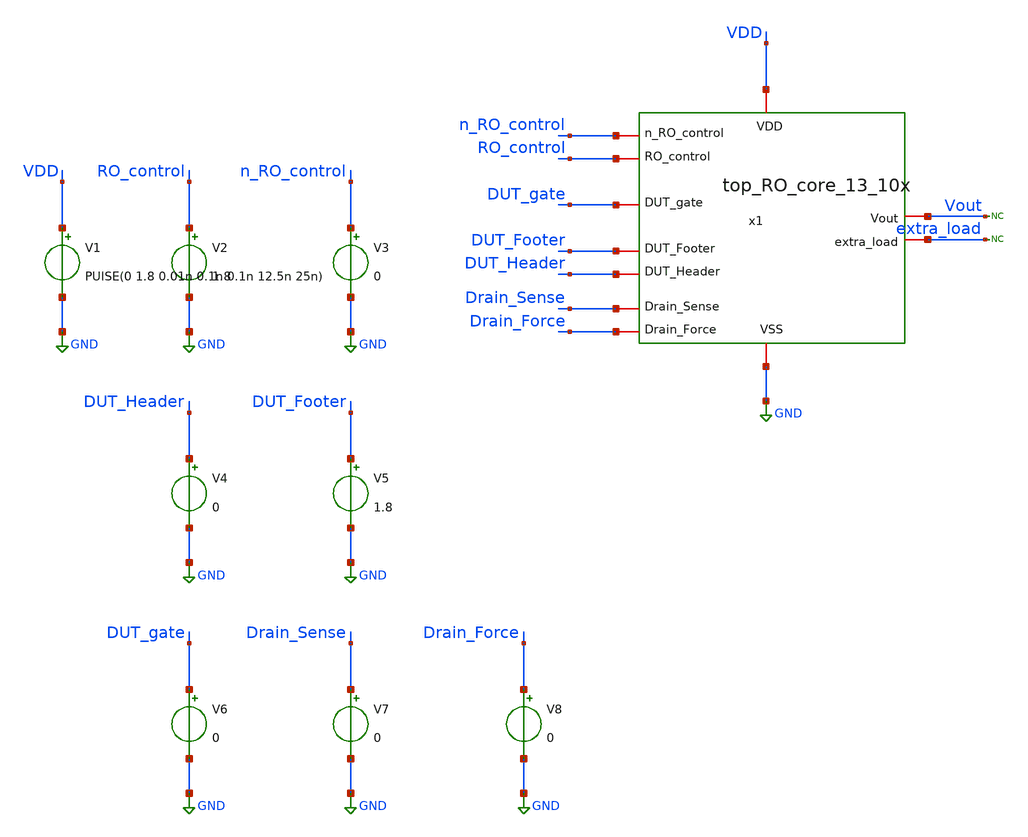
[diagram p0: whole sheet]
** sch_path: TT/top_RO_core_13_10x_tb.sch
.lib $::SKYWATER_MODELS/sky130.lib.spice tt
.include $::SKYWATER_STDCELLS/sky130_fd_sc_hd.spice

**.subckt top_RO_core_13_10x_tb
V1 VDD GND PUlSE(0 1.8 0.01n 0.1n 0.1n 12.5n 25n)
V2 RO_control GND 1.8
V3 n_RO_control GND 0
V4 DUT_Header GND 0
V5 DUT_Footer GND 1.8
* noconn extra_load
* noconn Vout
V6 DUT_gate GND 0
V7 Drain_Sense GND 0
V8 Drain_Force GND 0
x1 VDD GND n_RO_control RO_control DUT_gate Vout DUT_Header DUT_Footer Drain_Force Drain_Sense
+ extra_load top_RO_core_13_10x
**** begin user architecture code


.ic V(x1.A[8])=0.8
.tran 0.1n 50n
.save all



**** end user architecture code
**.ends

* expanding   symbol:  /foss/designs/Projects/RO_reliability/xschem/top_RO_core_13_10x.sym # of
*+ pins=11
** sym_path: TT/top_RO_core_13_10x.sym
** sch_path: TT/top_RO_core_13_10x.sch
.subckt top_RO_core_13_10x VDD VSS n_RO_control RO_control DUT_gate Vout DUT_Header DUT_Footer
+ Drain_Force Drain_Sense extra_load
*.iopin VDD
*.iopin VSS
*.iopin n_RO_control
*.iopin RO_control
*.iopin DUT_gate
*.iopin extra_load
*.iopin DUT_Header
*.iopin DUT_Footer
*.iopin Drain_Force
*.iopin Drain_Sense
*.iopin Vout
x1[1] VDD VSS A[8] A[7] rovcel2
x1[2] VDD VSS A[7] A[6] rovcel2
x1[3] VDD VSS A[6] A[5] rovcel2
x1[4] VDD VSS A[5] A[4] rovcel2
x1[5] VDD VSS A[4] A[3] rovcel2
x1[6] VDD VSS A[3] A[2] rovcel2
x1[7] VDD VSS A[2] A[1] rovcel2
x1[8] VDD VSS A[1] Vout rovcel2
x2 VDD VSS A[9] n_RO_control A_10 RO_control DUT_gate rovcel3
x3 VDD VSS A[9] A[8] rovcel2
x5 VDD VSS extra_load n_RO_control A_12 rovcel4
x6 VDD VSS Vout A_12 rovcel2
x1 DUT_Header DUT_Footer Drain_Force Drain_Sense RO_control n_RO_control VDD VSS A_10 extra_load
+ rovcel1_10
.ends


* expanding   symbol:  /foss/designs/Projects/RO_reliability/xschem/rovcel2.sym # of pins=4
** sym_path: TT/rovcel2.sym
** sch_path: TT/rovcel2.sch
.subckt rovcel2 VDD VSS Vout Vin
*.iopin VDD
*.iopin VSS
*.iopin Vin
*.iopin Vout
x1 VDD Vin Vout VSS inverter_RO_rel
x2 VDD VDD Vout net1 VSS VSS tgate
x3 VDD VDD Vout net2 VSS VSS tgate
* noconn #net1
* noconn #net2
.ends


* expanding   symbol:  /foss/designs/Projects/RO_reliability/xschem/rovcel3.sym # of pins=7
** sym_path: TT/rovcel3.sym
** sch_path: TT/rovcel3.sch
.subckt rovcel3 VDD VSS Vin n_RO_control Vout RO_control DUT_gate
*.iopin VDD
*.iopin VSS
*.iopin Vin
*.iopin n_RO_control
*.iopin RO_control
*.iopin DUT_gate
*.iopin Vout
* noconn #net1
x4 VDD VSS Vin n_RO_control RO_control Vout tristate_inv
x1 RO_control VDD Vout net1 VSS n_RO_control tgate
x5 RO_control VDD Vout DUT_gate VSS n_RO_control tgate
.ends


* expanding   symbol:  /foss/designs/Projects/RO_reliability/xschem/rovcel4.sym # of pins=5
** sym_path: TT/rovcel4.sym
** sch_path: TT/rovcel4.sch
.subckt rovcel4 VDD VSS Vin n_RO_control Vout
*.iopin VDD
*.iopin VSS
*.iopin Vin
*.iopin n_RO_control
*.iopin Vout
* noconn #net1
x4 n_RO_control VDD VSS Vin Vout inv1
x1 VDD VDD Vout VSS VSS VSS tgate
x5 VDD VDD Vout net1 VSS VSS tgate
.ends


* expanding   symbol:  /foss/designs/Projects/RO_reliability/xschem/rovcel1_10.sym # of pins=10
** sym_path: TT/rovcel1_10.sym
** sch_path: TT/rovcel1_10.sch
.subckt rovcel1_10 DUT_Header DUT_Footer Drain_Force Drain_Sense RO_control n_RO_control VDD VSS Vin
+ Vout
*.iopin VDD
*.iopin VSS
*.iopin Vin
*.iopin DUT_Header
*.iopin DUT_Footer
*.iopin Drain_Force
*.iopin Vout
*.iopin Drain_Sense
*.iopin RO_control
*.iopin n_RO_control
x1 VDD VSS Vin DUT_Header DUT_Footer Vout tristate_inv
x2 RO_control VDD Vout Drain_Sense VSS n_RO_control tgate
x3 RO_control VDD Vout Drain_Force VSS n_RO_control tgate_force10
.ends


* expanding   symbol:  /foss/designs/Projects/RO_reliability/xschem/inverter_RO_rel.sym # of pins=4
** sym_path: TT/inverter_RO_rel.sym
** sch_path: TT/inverter_RO_rel.sch
.subckt inverter_RO_rel VDD Vin Vout VSS
*.iopin VDD
*.iopin VSS
*.iopin Vin
*.iopin Vout
XM2 Vout Vin VDD VDD sky130_fd_pr__pfet_01v8 L=0.15 W=4.75 nf=1 ad='int((nf+1)/2) * W/nf * 0.29' as='int((nf+2)/2) * W/nf * 0.29'
+ pd='2*int((nf+1)/2) * (W/nf + 0.29)' ps='2*int((nf+2)/2) * (W/nf + 0.29)' nrd='0.29 / W' nrs='0.29 / W'
+ sa=0 sb=0 sd=0 mult=4 m=4
XM1 Vout Vin VSS VSS sky130_fd_pr__nfet_01v8 L=0.15 W=2.1 nf=1 ad='int((nf+1)/2) * W/nf * 0.29' as='int((nf+2)/2) * W/nf * 0.29'
+ pd='2*int((nf+1)/2) * (W/nf + 0.29)' ps='2*int((nf+2)/2) * (W/nf + 0.29)' nrd='0.29 / W' nrs='0.29 / W'
+ sa=0 sb=0 sd=0 mult=2 m=2
.ends


* expanding   symbol:  /foss/designs/Projects/RO_reliability/xschem/tgate.sym # of pins=6
** sym_path: TT/tgate.sym
** sch_path: TT/tgate.sch
.subckt tgate nclk VDD Vin Vout VSS clk
*.iopin nclk
*.iopin clk
*.iopin VDD
*.iopin VSS
*.iopin Vout
*.iopin Vin
XM1 Vin nclk Vout VDD sky130_fd_pr__pfet_01v8 L=0.15 W=0.45 nf=1 ad='int((nf+1)/2) * W/nf * 0.29' as='int((nf+2)/2) * W/nf * 0.29'
+ pd='2*int((nf+1)/2) * (W/nf + 0.29)' ps='2*int((nf+2)/2) * (W/nf + 0.29)' nrd='0.29 / W' nrs='0.29 / W'
+ sa=0 sb=0 sd=0 mult=1 m=1
XM2 Vin clk Vout VSS sky130_fd_pr__nfet_01v8 L=0.15 W=0.45 nf=1 ad='int((nf+1)/2) * W/nf * 0.29' as='int((nf+2)/2) * W/nf * 0.29'
+ pd='2*int((nf+1)/2) * (W/nf + 0.29)' ps='2*int((nf+2)/2) * (W/nf + 0.29)' nrd='0.29 / W' nrs='0.29 / W'
+ sa=0 sb=0 sd=0 mult=1 m=1
.ends


* expanding   symbol:  /foss/designs/RO_Aging_UNICASS/TT/tristate_inv.sym # of pins=6
** sym_path: TT/tristate_inv.sym
** sch_path: TT/tristate_inv.sch
.subckt tristate_inv VDD VSS Vin Vup Vdn Vout
*.iopin VDD
*.iopin VSS
*.iopin Vin
*.iopin Vout
*.iopin Vup
*.iopin Vdn
XM1 net1 Vup VDD VDD sky130_fd_pr__pfet_01v8 L=0.15 W=4.75 nf=1 ad='int((nf+1)/2) * W/nf * 0.29' as='int((nf+2)/2) * W/nf * 0.29'
+ pd='2*int((nf+1)/2) * (W/nf + 0.29)' ps='2*int((nf+2)/2) * (W/nf + 0.29)' nrd='0.29 / W' nrs='0.29 / W'
+ sa=0 sb=0 sd=0 mult=40 m=40
XM2 Vout Vin net1 VDD sky130_fd_pr__pfet_01v8 L=0.15 W=4.75 nf=1 ad='int((nf+1)/2) * W/nf * 0.29' as='int((nf+2)/2) * W/nf * 0.29'
+ pd='2*int((nf+1)/2) * (W/nf + 0.29)' ps='2*int((nf+2)/2) * (W/nf + 0.29)' nrd='0.29 / W' nrs='0.29 / W'
+ sa=0 sb=0 sd=0 mult=4 m=4
XM3 Vout Vin net2 VSS sky130_fd_pr__nfet_01v8 L=0.15 W=2.1 nf=1 ad='int((nf+1)/2) * W/nf * 0.29' as='int((nf+2)/2) * W/nf * 0.29'
+ pd='2*int((nf+1)/2) * (W/nf + 0.29)' ps='2*int((nf+2)/2) * (W/nf + 0.29)' nrd='0.29 / W' nrs='0.29 / W'
+ sa=0 sb=0 sd=0 mult=2 m=2
XM4 net2 Vdn VSS VSS sky130_fd_pr__nfet_01v8 L=0.15 W=2.1 nf=1 ad='int((nf+1)/2) * W/nf * 0.29' as='int((nf+2)/2) * W/nf * 0.29'
+ pd='2*int((nf+1)/2) * (W/nf + 0.29)' ps='2*int((nf+2)/2) * (W/nf + 0.29)' nrd='0.29 / W' nrs='0.29 / W'
+ sa=0 sb=0 sd=0 mult=20 m=20
.ends


* expanding   symbol:  /foss/designs/RO_Aging_UNICASS/TT/inv1.sym # of pins=5
** sym_path: TT/inv1.sym
** sch_path: TT/inv1.sch
.subckt inv1 n_RO_control VDD VSS Vin Vout
*.iopin VDD
*.iopin VSS
*.iopin Vin
*.iopin Vout
*.iopin n_RO_control
XM1 net1 n_RO_control VDD VDD sky130_fd_pr__pfet_01v8 L=0.15 W=4.75 nf=1 ad='int((nf+1)/2) * W/nf * 0.29'
+ as='int((nf+2)/2) * W/nf * 0.29' pd='2*int((nf+1)/2) * (W/nf + 0.29)' ps='2*int((nf+2)/2) * (W/nf + 0.29)'
+ nrd='0.29 / W' nrs='0.29 / W' sa=0 sb=0 sd=0 mult=40 m=40
XM2 Vout Vin net1 VDD sky130_fd_pr__pfet_01v8 L=0.15 W=4.75 nf=1 ad='int((nf+1)/2) * W/nf * 0.29' as='int((nf+2)/2) * W/nf * 0.29'
+ pd='2*int((nf+1)/2) * (W/nf + 0.29)' ps='2*int((nf+2)/2) * (W/nf + 0.29)' nrd='0.29 / W' nrs='0.29 / W'
+ sa=0 sb=0 sd=0 mult=4 m=4
XM3 Vout Vin VSS VSS sky130_fd_pr__nfet_01v8 L=0.15 W=2.1 nf=1 ad='int((nf+1)/2) * W/nf * 0.29' as='int((nf+2)/2) * W/nf * 0.29'
+ pd='2*int((nf+1)/2) * (W/nf + 0.29)' ps='2*int((nf+2)/2) * (W/nf + 0.29)' nrd='0.29 / W' nrs='0.29 / W'
+ sa=0 sb=0 sd=0 mult=2 m=2
.ends


* expanding   symbol:  /foss/designs/Projects/RO_reliability/xschem/tgate_force10.sym # of pins=6
** sym_path: TT/tgate_force10.sym
** sch_path: TT/tgate_force10.sch
.subckt tgate_force10 nclk VDD Vin Vout VSS clk
*.iopin nclk
*.iopin clk
*.iopin VDD
*.iopin VSS
*.iopin Vout
*.iopin Vin
XM1 Vin nclk Vout VDD sky130_fd_pr__pfet_01v8 L=0.15 W=4.75 nf=1 ad='int((nf+1)/2) * W/nf * 0.29' as='int((nf+2)/2) * W/nf * 0.29'
+ pd='2*int((nf+1)/2) * (W/nf + 0.29)' ps='2*int((nf+2)/2) * (W/nf + 0.29)' nrd='0.29 / W' nrs='0.29 / W'
+ sa=0 sb=0 sd=0 mult=40 m=40
XM2 Vin clk Vout VSS sky130_fd_pr__nfet_01v8 L=0.15 W=2.1 nf=1 ad='int((nf+1)/2) * W/nf * 0.29' as='int((nf+2)/2) * W/nf * 0.29'
+ pd='2*int((nf+1)/2) * (W/nf + 0.29)' ps='2*int((nf+2)/2) * (W/nf + 0.29)' nrd='0.29 / W' nrs='0.29 / W'
+ sa=0 sb=0 sd=0 mult=20 m=20
.ends

.GLOBAL GND
.end
